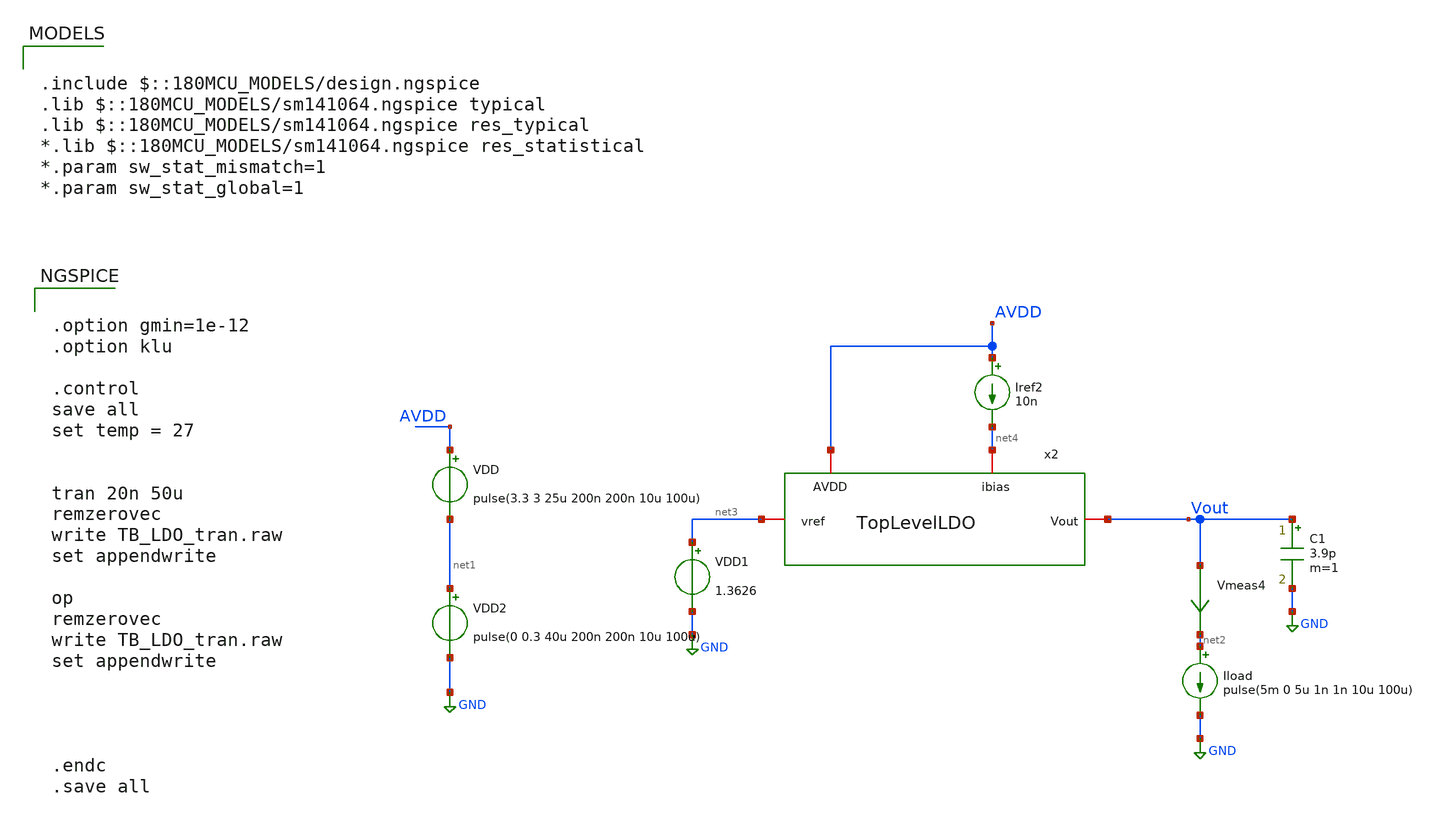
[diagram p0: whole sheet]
** sch_path: Voltage_Reference/LDO/TB_LDO_tran.sch
**.subckt TB_LDO_tran
VDD AVDD net1 pulse(3.3 3 25u 200n 200n 10u 100u)
Iload net2 GND pulse(5m 0 5u 1n 1n 10u 100u)
Vmeas4 Vout net2 0
.save i(vmeas4)
VDD1 net3 GND 1.3626
VDD2 net1 GND pulse(0 0.3 40u 200n 200n 10u 100u)
Iref2 AVDD net4 10n
x2 AVDD net4 net3 Vout TopLevelLDO
C1 Vout GND 3.9p m=1
**** begin user architecture code

.include $::180MCU_MODELS/design.ngspice
.lib $::180MCU_MODELS/sm141064.ngspice typical
.lib $::180MCU_MODELS/sm141064.ngspice res_typical
*.lib $::180MCU_MODELS/sm141064.ngspice res_statistical
*.param sw_stat_mismatch=1
*.param sw_stat_global=1



.option gmin=1e-12
.option klu

.control
save all
set temp = 27


tran 20n 50u
remzerovec
write TB_LDO_tran.raw
set appendwrite

op
remzerovec
write TB_LDO_tran.raw
set appendwrite




.endc
.save all


**** end user architecture code
**.ends
.GLOBAL GND
.end
